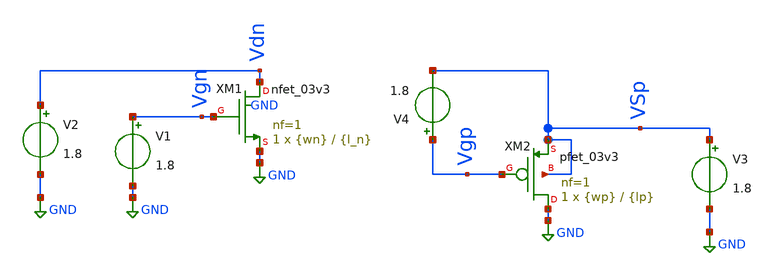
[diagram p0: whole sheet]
** sch_path: xschem/caracterizador/charac.sch
* Copyright 2022 GlobalFoundries PDK Authors
* Licensed under the Apache License, Version 2.0 (the "License");
* you may not use this file except in compliance with the License.
* You may obtain a copy of the License at
* https://www.apache.org/licenses/LICENSE-2.0
* Unless required by applicable law or agreed to in writing, software
* distributed under the License is distributed on an "AS IS" BASIS,
* WITHOUT WARRANTIES OR CONDITIONS OF ANY KIND, either express or implied.
* See the License for the specific language governing permissions and
* limitations under the License.
**.subckt charac
XM1 Vdn Vgn GND GND nfet_03v3 L={l_n} W={wn} nf=1 ad='int((nf+1)/2) * W/nf * 0.18u' as='int((nf+2)/2) * W/nf * 0.18u'
+ pd='2*int((nf+1)/2) * (W/nf + 0.18u)' ps='2*int((nf+2)/2) * (W/nf + 0.18u)' nrd='0.18u / W' nrs='0.18u / W'
+ sa=0 sb=0 sd=0 m=1 par=1
XM2 GND Vgp VSp VSp pfet_03v3 L={lp} W={wp} nf=1 ad='int((nf+1)/2) * W/nf * 0.18u' as='int((nf+2)/2) * W/nf * 0.18u'
+ pd='2*int((nf+1)/2) * (W/nf + 0.18u)' ps='2*int((nf+2)/2) * (W/nf + 0.18u)' nrd='0.18u / W' nrs='0.18u / W'
+ sa=0 sb=0 sd=0 m=1 par=1
V1 Vgn GND 1.8
V2 Vdn GND 1.8
V3 VSp GND 1.8
V4 Vgp VSp 1.8
**** begin user architecture code


.include /home/ringosinye/eda/pdks/gf180mcuD/libs.tech/ngspice/design.ngspice
.lib /home/ringosinye/eda/pdks/gf180mcuD/libs.tech/ngspice/sm141064.ngspice typical
.param sw_stat_mismatch = 0
.param wn=1u l_n=1u wp=1u lp=1u




.control

* ==================================================================
* 1. PARAMETROS EDITABLES
* ==================================================================
* --- NMOS: dimensiones (m), VDS fijo (V) y punto objetivo gm/ID ---
set wn_val     = 10e-6
set ln_val     = 1e-6
set vds_fijo_n = 1.65
set gmro_obj_n = 300

* --- PMOS: dimensiones (m), VSD fijo (V) y punto objetivo gm/ID ---
set wp_val     = 10e-6
set lp_val     = 1e-6
set vsd_fijo_p = 1.65
set gmro_obj_p = 300

* Aplicar geometria al esquematico
alterparam wn=$wn_val
alterparam l_n=$ln_val
alterparam wp=$wp_val
alterparam lp=$lp_val
reset

* Guardar nodos y parametros internos BSIM4 necesarios para el barrido
save all

* Guardar parámetros internos del NMOS (XM1)
save @m.xm1.m0[id]
save @m.xm1.m0[vth]
save @m.xm1.m0[vdsat]
save @m.xm1.m0[gm]
save @m.xm1.m0[gds]
*save @m.xm1.m0[gmbs]
*save @m.xm1.m0[cgg]
*save @m.xm1.m0[cgs]
*save @m.xm1.m0[cgd]

*Guardar parámetros internos del PMOS (XM2)
save @m.xm2.m0[id]
save @m.xm2.m0[vth]
save @m.xm2.m0[vdsat]
save @m.xm2.m0[gm]
*save @m.xm2.m0[gds]
*save @m.xm2.m0[gmbs]
*save @m.xm2.m0[cgg]
*save @m.xm2.m0[cgs]
*save @m.xm2.m0[cgd]

* ======================= ESTILO DE GRAFICOS =======================
set color0=white
set color1=black
set color2=blue
set color3=red
set color4=darkgreen
set xbrushwidth=2

* ==================================================================
* 2. NMOS: BARRIDO gm/ID vs VGS (a VDS fijo)
* ==================================================================
alter v2 $vds_fijo_n
dc V1 0.1 3.3 0.005

let id_n = abs(@m.xm1.m0[id])
let gm_n    = abs(@m.xm1.m0[gm])
let gds_n    = abs(@m.xm1.m0[gds])
let gmid_n  = gm_n / id_n
let gmro_n = gm_n/gds_n
let vdsat_n = abs(@m.xm1.m0[vdsat])
let vth_n   = abs(@m.xm1.m0[vth])
let ref_n   = $gmro_obj_n + 0*gmro_n

* Extraccion del punto especifico donde gm/ID = gmid_obj_n
meas dc vgs_pt_n find v(vgn) when gmro_n=$gmro_obj_n

set vgs_pn   = $&vgs_pt_n

plot gmro_n ref_n title 'NMOS: gmro vs VGS' xlabel 'VGS (V)' ylabel 'gmro (V/V)'

* ==================================================================
* 3. PMOS: BARRIDO gm/ID vs VSG (a VSD fijo)
* ==================================================================
alter v3 $vsd_fijo_p
dc V4 -0.1 -3.3 -0.005

let vsg_p   = abs(v(vgp) - v(vsp))
let id_p    = abs(@m.xm2.m0[id]) + 1e-18
let gm_p    = abs(@m.xm2.m0[gm])
let gds_p   = abs(@m.xm2.m0[gds])
let gmro_p = gm_p/gdp_n
let gmid_p  = gm_p / id_p
let vdsat_p = abs(@m.xm2.m0[vdsat])
let vth_p   = abs(@m.xm2.m0[vth])
let ref_p   = $gmro_obj_p + 0*gmro_p

* Extraccion del punto especifico donde gm/ID = gmid_obj_p
meas dc vsg_pt_p find vsg_p when gmro_p=$gmro_obj_p

set vsg_pp   = $&vsg_pt_p

plot gmro_p ref_p vs vsg_p title 'PMOS: gmro vs VSG' xlabel 'VSG (V)' ylabel 'gmro (V/V)'

* ==================================================================
* 4. REPORTE NUMERICO EN CONSOLA
* ==================================================================
echo ==========================================================
echo  NMOS (W=$wn_val, L=$ln_val, VDS=$vds_fijo_n V) -- gmro = $gmro_obj_n V/V
echo ==========================================================
echo  VGS requerido = $vgs_pn V
echo ==========================================================
echo
echo ==========================================================
echo  PMOS (W=$wp_val, L=$lp_val, VSD=$vsd_fijo_p V) -- gmro = $gmro_obj_p V/V
echo ==========================================================
echo  VSG requerido = $vsg_pp V
echo ==========================================================
.endc


**** end user architecture code
**.ends
.GLOBAL GND
.end
